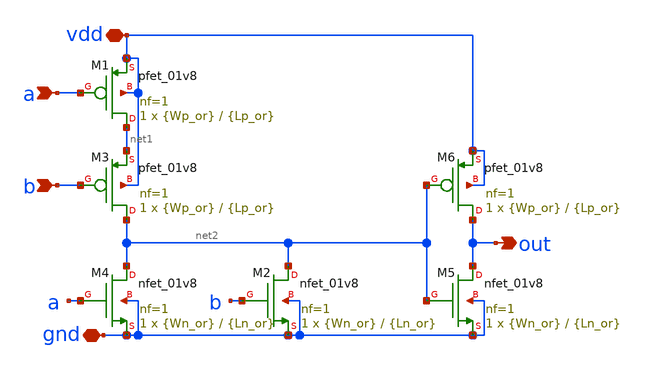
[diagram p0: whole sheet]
** sch_path: inhibitory/or_2.sch
**.subckt or_2 gnd a b out vdd
*.iopin gnd
*.ipin a
*.ipin b
*.opin out
*.iopin vdd
XM1 net1 a vdd vdd sky130_fd_pr__pfet_01v8 L={Lp_or} W={Wp_or} nf=1 ad='int((nf+1)/2) * W/nf * 0.29'
+ as='int((nf+2)/2) * W/nf * 0.29' pd='2*int((nf+1)/2) * (W/nf + 0.29)' ps='2*int((nf+2)/2) * (W/nf + 0.29)'
+ nrd='0.29 / W' nrs='0.29 / W' sa=0 sb=0 sd=0 mult=1 m=1
XM2 net2 b gnd gnd sky130_fd_pr__nfet_01v8 L={Ln_or} W={Wn_or} nf=1 ad='int((nf+1)/2) * W/nf * 0.29'
+ as='int((nf+2)/2) * W/nf * 0.29' pd='2*int((nf+1)/2) * (W/nf + 0.29)' ps='2*int((nf+2)/2) * (W/nf + 0.29)'
+ nrd='0.29 / W' nrs='0.29 / W' sa=0 sb=0 sd=0 mult=1 m=1
XM3 net2 b net1 vdd sky130_fd_pr__pfet_01v8 L={Lp_or} W={Wp_or} nf=1 ad='int((nf+1)/2) * W/nf * 0.29'
+ as='int((nf+2)/2) * W/nf * 0.29' pd='2*int((nf+1)/2) * (W/nf + 0.29)' ps='2*int((nf+2)/2) * (W/nf + 0.29)'
+ nrd='0.29 / W' nrs='0.29 / W' sa=0 sb=0 sd=0 mult=1 m=1
XM4 net2 a gnd gnd sky130_fd_pr__nfet_01v8 L={Ln_or} W={Wn_or} nf=1 ad='int((nf+1)/2) * W/nf * 0.29'
+ as='int((nf+2)/2) * W/nf * 0.29' pd='2*int((nf+1)/2) * (W/nf + 0.29)' ps='2*int((nf+2)/2) * (W/nf + 0.29)'
+ nrd='0.29 / W' nrs='0.29 / W' sa=0 sb=0 sd=0 mult=1 m=1
XM5 out net2 gnd gnd sky130_fd_pr__nfet_01v8 L={Ln_or} W={Wn_or} nf=1 ad='int((nf+1)/2) * W/nf * 0.29'
+ as='int((nf+2)/2) * W/nf * 0.29' pd='2*int((nf+1)/2) * (W/nf + 0.29)' ps='2*int((nf+2)/2) * (W/nf + 0.29)'
+ nrd='0.29 / W' nrs='0.29 / W' sa=0 sb=0 sd=0 mult=1 m=1
XM6 out net2 vdd vdd sky130_fd_pr__pfet_01v8 L={Lp_or} W={Wp_or} nf=1 ad='int((nf+1)/2) * W/nf * 0.29'
+ as='int((nf+2)/2) * W/nf * 0.29' pd='2*int((nf+1)/2) * (W/nf + 0.29)' ps='2*int((nf+2)/2) * (W/nf + 0.29)'
+ nrd='0.29 / W' nrs='0.29 / W' sa=0 sb=0 sd=0 mult=1 m=1
**.ends
.end
